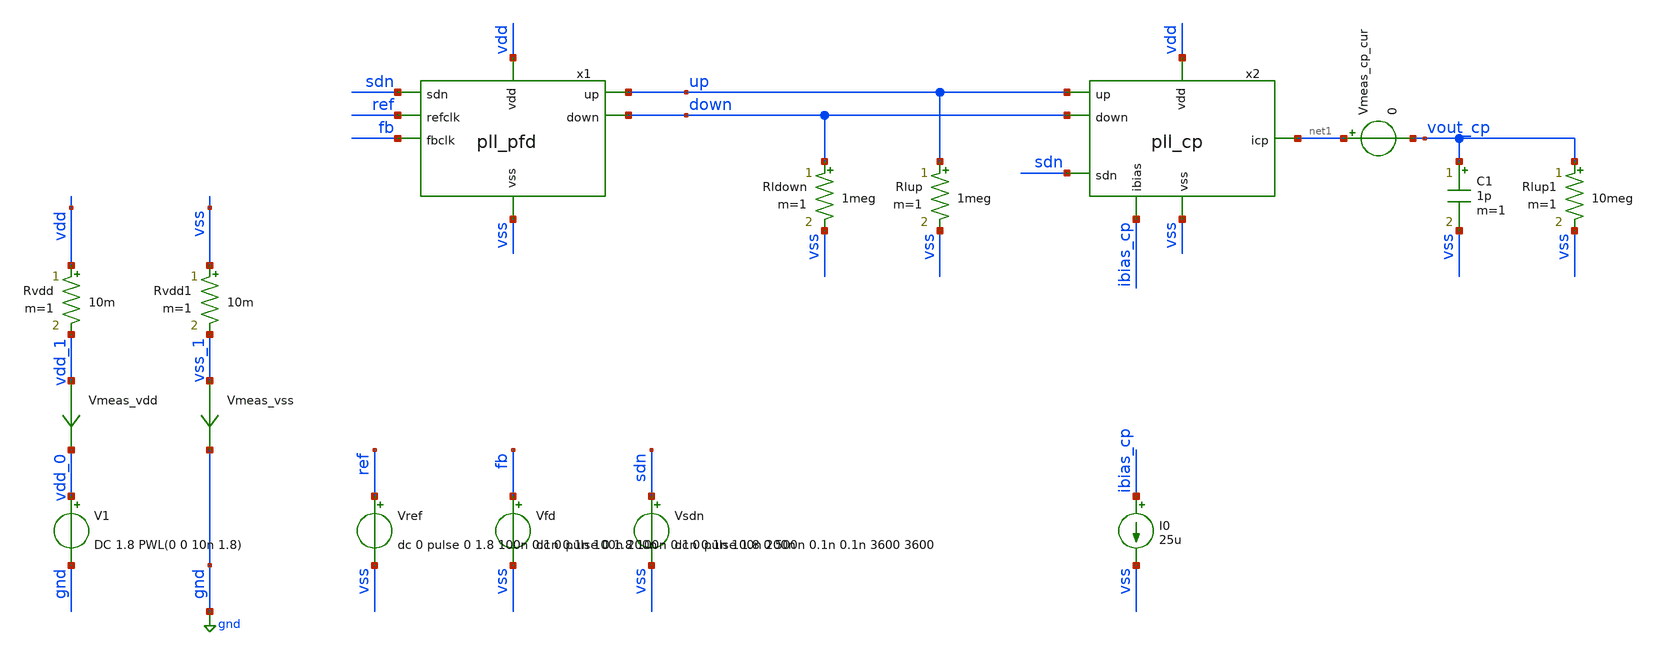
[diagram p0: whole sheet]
** sch_path: pll/pll_cp/simulation/pll_cp_tb.sch
**.subckt pll_cp_tb
V1 vdd_0 gnd DC 1.8 PWL(0 0 10n 1.8)
Vmeas_vdd vdd_1 vdd_0 0
.save i(vmeas_vdd)
Vref ref vss dc 0 pulse 0 1.8 100n 0.1n 0.1n 100n 200n
Vfd fb vss dc 0 pulse 0 1.8 100n 0.1n 0.1n 100n 200n
Vsdn sdn vss dc 0 pulse 1.8 0 500n 0.1n 0.1n 3600 3600
Vmeas_vss vss_1 gnd 0
.save i(vmeas_vss)
Rvdd vdd vdd_1 10m m=1
Rvdd1 vss vss_1 10m m=1
Rlup up vss 1meg m=1
Rldown down vss 1meg m=1
I0 ibias_cp vss 25u
Vmeas_cp_cur net1 vout_cp 0
Rlup1 vout_cp vss 10meg m=1
C1 vout_cp vss 1p m=1
x1 ref up sdn fb down vdd vss pll_pfd
x2 vdd up net1 ibias_cp down sdn vss pll_cp
**** begin user architecture code



.option savecurrents
*.option rshunt = 1e12
*.option gmin = 1e-24

** Settings for PSS osciallator
*.option reltol=1e-5
*.option vntol=3e-8
*.option abstol=1e-13
**.option chgtol=1e-12
*.option trtol=10
.option method=gear

.control

* #################################################################
* #
* #                         OPERATING POINT
* #
* #################################################################
reset
save all

op
set filetype=binary
write pll_cp_tb.raw all

* #################################################################
* #
* #                 TRANSIENT OSCILATION REGIME
* #
* #################################################################
reset
setplot const
save all
save v(ref)
save v(fb)
save v(sdn)
save v(up) v(up2)
save v(vout_cp)
save i(Vmeas_cp_cur)
save i(v.x2.Vcp1) i(v.x2.Vcp2)

tran 0.05n 2u uic
set filetype=ascii
write pll_cp_tb_tran.raw v(ref) v(fb) v(sdn) v(up) v(down)

* Plot outputs
plot v(sdn)+10 v(ref)+8 v(fb)+6 v(up)+4 v(down)+2 v(vout_cp)

*rusage
.endc



.options wnflag=1
.include $::SKYWATER_MODELS/cells/nfet_01v8/sky130_fd_pr__nfet_01v8__tt.corner.spice
.include $::SKYWATER_MODELS/cells/nfet_01v8_lvt/sky130_fd_pr__nfet_01v8_lvt__tt.corner.spice
.include $::SKYWATER_MODELS/cells/pfet_01v8/sky130_fd_pr__pfet_01v8__tt.corner.spice
.include $::SKYWATER_MODELS/cells/nfet_03v3_nvt/sky130_fd_pr__nfet_03v3_nvt__tt.corner.spice
.include $::SKYWATER_MODELS/cells/nfet_05v0_nvt/sky130_fd_pr__nfet_05v0_nvt__tt.corner.spice
.include $::SKYWATER_MODELS/cells/esd_nfet_01v8/sky130_fd_pr__esd_nfet_01v8__tt.corner.spice
.include $::SKYWATER_MODELS/cells/pfet_01v8_lvt/sky130_fd_pr__pfet_01v8_lvt__tt.corner.spice
.include $::SKYWATER_MODELS/cells/pfet_01v8_hvt/sky130_fd_pr__pfet_01v8_hvt__tt.corner.spice
.include $::SKYWATER_MODELS/cells/esd_pfet_g5v0d10v5/sky130_fd_pr__esd_pfet_g5v0d10v5__tt.corner.spice
.include $::SKYWATER_MODELS/cells/pfet_g5v0d10v5/sky130_fd_pr__pfet_g5v0d10v5__tt.corner.spice
.include $::SKYWATER_MODELS/cells/pfet_g5v0d16v0/sky130_fd_pr__pfet_g5v0d16v0__tt.corner.spice
.include $::SKYWATER_MODELS/cells/nfet_g5v0d10v5/sky130_fd_pr__nfet_g5v0d10v5__tt.corner.spice
.include $::SKYWATER_MODELS/cells/nfet_g5v0d16v0/sky130_fd_pr__nfet_g5v0d16v0__tt_discrete.corner.spice
.include $::SKYWATER_MODELS/cells/esd_nfet_g5v0d10v5/sky130_fd_pr__esd_nfet_g5v0d10v5__tt.corner.spice
.include $::SKYWATER_MODELS/models/corners/tt/nonfet.spice

.include $::SKYWATER_MODELS/cells/cap_var_hvt/sky130_fd_pr__cap_var_hvt.model.spice

* Mismatch parameters
.include $::SKYWATER_MODELS/cells/nfet_01v8/sky130_fd_pr__nfet_01v8__mismatch.corner.spice
.include $::SKYWATER_MODELS/cells/pfet_01v8/sky130_fd_pr__pfet_01v8__mismatch.corner.spice
.include $::SKYWATER_MODELS/cells/nfet_01v8_lvt/sky130_fd_pr__nfet_01v8_lvt__mismatch.corner.spice
.include $::SKYWATER_MODELS/cells/pfet_01v8_lvt/sky130_fd_pr__pfet_01v8_lvt__mismatch.corner.spice
.include $::SKYWATER_MODELS/cells/pfet_01v8_hvt/sky130_fd_pr__pfet_01v8_hvt__mismatch.corner.spice
.include $::SKYWATER_MODELS/cells/nfet_g5v0d10v5/sky130_fd_pr__nfet_g5v0d10v5__mismatch.corner.spice
.include $::SKYWATER_MODELS/cells/pfet_g5v0d10v5/sky130_fd_pr__pfet_g5v0d10v5__mismatch.corner.spice
.include $::SKYWATER_MODELS/cells/nfet_05v0_nvt/sky130_fd_pr__nfet_05v0_nvt__mismatch.corner.spice
.include $::SKYWATER_MODELS/cells/nfet_03v3_nvt/sky130_fd_pr__nfet_03v3_nvt__mismatch.corner.spice

* Resistor$::SKYWATER_MODELS/Capacitor
.include $::SKYWATER_MODELS/models/r+c/res_typical__cap_typical.spice
.include $::SKYWATER_MODELS/models/r+c/res_typical__cap_typical__lin.spice

* Special cells
.include $::SKYWATER_MODELS/models/corners/tt/specialized_cells.spice

* All models
.include $::SKYWATER_MODELS/models/all.spice

* Corner
.include $::SKYWATER_MODELS/models/corners/tt/rf.spice

* .include $::SKYWATER_STDCELLS/cells/
.include $::SKYWATER_STDCELLS/cells/buf/sky130_fd_sc_hd__buf_1.spice
.include $::SKYWATER_STDCELLS_HS/cells/buf/sky130_fd_sc_hs__buf_1.spice
.include $::SKYWATER_STDCELLS_HS/cells/buf/sky130_fd_sc_hs__buf_16.spice
.include $::SKYWATER_STDCELLS/cells/clkbuf/sky130_fd_sc_hd__clkbuf_1.spice
.include $::SKYWATER_STDCELLS/cells/clkbuf/sky130_fd_sc_hd__clkbuf_2.spice
.include $::SKYWATER_STDCELLS/cells/clkbuf/sky130_fd_sc_hd__clkbuf_4.spice
.include $::SKYWATER_STDCELLS/cells/clkbuf/sky130_fd_sc_hd__clkbuf_8.spice
.include $::SKYWATER_STDCELLS/cells/clkbuf/sky130_fd_sc_hd__clkbuf_16.spice
.include $::SKYWATER_STDCELLS/cells/decap/sky130_fd_sc_hd__decap_3.spice
.include $::SKYWATER_STDCELLS/cells/decap/sky130_fd_sc_hd__decap_4.spice
.include $::SKYWATER_STDCELLS/cells/decap/sky130_fd_sc_hd__decap_8.spice
.include $::SKYWATER_STDCELLS/cells/dfrbp/sky130_fd_sc_hd__dfrbp_1.spice
.include $::SKYWATER_STDCELLS/cells/dfrbp/sky130_fd_sc_hd__dfrbp_2.spice
.include $::SKYWATER_STDCELLS/cells/inv/sky130_fd_sc_hd__inv_1.spice
.include $::SKYWATER_STDCELLS/cells/inv/sky130_fd_sc_hd__inv_2.spice
.include $::SKYWATER_STDCELLS/cells/inv/sky130_fd_sc_hd__inv_4.spice
.include $::SKYWATER_STDCELLS/cells/inv/sky130_fd_sc_hd__inv_8.spice
.include $::SKYWATER_STDCELLS/cells/inv/sky130_fd_sc_hd__inv_16.spice
.include $::SKYWATER_STDCELLS_HS/cells/inv/sky130_fd_sc_hs__inv_1.spice
.include $::SKYWATER_STDCELLS_HS/cells/inv/sky130_fd_sc_hs__inv_2.spice
.include $::SKYWATER_STDCELLS_HS/cells/inv/sky130_fd_sc_hs__inv_4.spice
.include $::SKYWATER_STDCELLS_HS/cells/inv/sky130_fd_sc_hs__inv_8.spice
.include $::SKYWATER_STDCELLS_HS/cells/inv/sky130_fd_sc_hs__inv_16.spice
.include $::SKYWATER_STDCELLS/cells/mux2/sky130_fd_sc_hd__mux2_2.spice
.include $::SKYWATER_STDCELLS/cells/nand2/sky130_fd_sc_hd__nand2_1.spice
.include $::SKYWATER_STDCELLS/cells/tap/sky130_fd_sc_hd__tap_2.spice
.include $::SKYWATER_STDCELLS/cells/tapvpwrvgnd/sky130_fd_sc_hd__tapvpwrvgnd_1.spice

**** end user architecture code
**.ends

* expanding   symbol:  test_jens/pll/pll_pfd/pll_pfd.sym # of pins=7
** sym_path: pll/pll_pfd/xschem/pll_pfd.sym
** sch_path: pll/pll_pfd/xschem/pll_pfd.sch
.subckt pll_pfd refclk up sdn fbclk down vdd vss
*.ipin refclk
*.ipin fbclk
*.opin up
*.opin down
*.ipin sdn
*.ipin vdd
*.ipin vss
x1 refclk vdd rst_3 vss vss vdd vdd up up_inv sky130_fd_sc_hd__dfrbp_2
x2 fbclk vdd rst_3 vss vss vdd vdd down down_inv sky130_fd_sc_hd__dfrbp_2
x6 rst_2 sdn_inv vss vss vdd vdd rst_3 sky130_fd_sc_hd__and2_2
x4 rst_0 vss vss vdd vdd rst_1 sky130_fd_sc_hd__buf_1
x5 rst_1 vss vss vdd vdd rst_2 sky130_fd_sc_hd__buf_1
x7 sdn vss vss vdd vdd sdn_inv sky130_fd_sc_hd__inv_1
**** begin user architecture code
* .include $::SKYWATER_STDCELLS/cells/
.include $::SKYWATER_STDCELLS/cells/and2/sky130_fd_sc_hd__and2_1.spice
.include $::SKYWATER_STDCELLS/cells/and2/sky130_fd_sc_hd__and2_2.spice
.include $::SKYWATER_STDCELLS_HS/cells/and2/sky130_fd_sc_hs__and2_1.spice
.include $::SKYWATER_STDCELLS_HS/cells/and2/sky130_fd_sc_hs__and2_2.spice

.include $::SKYWATER_STDCELLS/cells/or2/sky130_fd_sc_hd__or2_1.spice
.include $::SKYWATER_STDCELLS/cells/or2/sky130_fd_sc_hd__or2_2.spice
.include $::SKYWATER_STDCELLS_HS/cells/or2/sky130_fd_sc_hs__or2_1.spice
.include $::SKYWATER_STDCELLS_HS/cells/or2/sky130_fd_sc_hs__or2_2.spice

.include $::SKYWATER_STDCELLS/cells/buf/sky130_fd_sc_hd__buf_1.spice
.include $::SKYWATER_STDCELLS_HS/cells/buf/sky130_fd_sc_hs__buf_1.spice

.include $::SKYWATER_STDCELLS/cells/dfrbp/sky130_fd_sc_hd__dfrbp_1.spice
.include $::SKYWATER_STDCELLS/cells/dfrbp/sky130_fd_sc_hd__dfrbp_2.spice
.include $::SKYWATER_STDCELLS_HS/cells/dfrbp/sky130_fd_sc_hs__dfrbp_1.spice
.include $::SKYWATER_STDCELLS_HS/cells/dfrbp/sky130_fd_sc_hs__dfrbp_2.spice

.include $::SKYWATER_STDCELLS/cells/inv/sky130_fd_sc_hd__inv_1.spice
.include $::SKYWATER_STDCELLS/cells/inv/sky130_fd_sc_hd__inv_2.spice
.include $::SKYWATER_STDCELLS/cells/inv/sky130_fd_sc_hd__inv_4.spice
.include $::SKYWATER_STDCELLS/cells/inv/sky130_fd_sc_hd__inv_8.spice
.include $::SKYWATER_STDCELLS/cells/inv/sky130_fd_sc_hd__inv_16.spice
.include $::SKYWATER_STDCELLS_HS/cells/inv/sky130_fd_sc_hs__inv_1.spice
.include $::SKYWATER_STDCELLS_HS/cells/inv/sky130_fd_sc_hs__inv_2.spice
.include $::SKYWATER_STDCELLS_HS/cells/inv/sky130_fd_sc_hs__inv_4.spice
.include $::SKYWATER_STDCELLS_HS/cells/inv/sky130_fd_sc_hs__inv_8.spice
.include $::SKYWATER_STDCELLS_HS/cells/inv/sky130_fd_sc_hs__inv_16.spice

.include $::SKYWATER_STDCELLS/cells/mux2/sky130_fd_sc_hd__mux2_2.spice
.include $::SKYWATER_STDCELLS/cells/nand2/sky130_fd_sc_hd__nand2_1.spice

.include $::SKYWATER_STDCELLS/cells/tap/sky130_fd_sc_hd__tap_2.spice
.include $::SKYWATER_STDCELLS/cells/tapvpwrvgnd/sky130_fd_sc_hd__tapvpwrvgnd_1.spice

**** end user architecture code
x3 up_inv down_inv vss vss vdd vdd rst_0 sky130_fd_sc_hd__or2_1
* noconn vss
* noconn vdd
.ends


* expanding   symbol:  test_jens/pll/pll_cp/pll_cp.sym # of pins=7
** sym_path: pll/pll_cp/xschem/pll_cp.sym
** sch_path: pll/pll_cp/xschem/pll_cp.sch
.subckt pll_cp vdd up icp ibias down sdn vss
*.ipin vdd
*.ipin vss
*.ipin up
*.ipin down
*.ipin ibias
*.ipin sdn
*.opin icp
**** begin user architecture code
* .include $::SKYWATER_STDCELLS/cells/
.include $::SKYWATER_STDCELLS/cells/and2/sky130_fd_sc_hd__and2_1.spice
.include $::SKYWATER_STDCELLS/cells/and2/sky130_fd_sc_hd__and2_2.spice
.include $::SKYWATER_STDCELLS_HS/cells/and2/sky130_fd_sc_hs__and2_1.spice
.include $::SKYWATER_STDCELLS_HS/cells/and2/sky130_fd_sc_hs__and2_2.spice

.include $::SKYWATER_STDCELLS/cells/or2/sky130_fd_sc_hd__or2_1.spice
.include $::SKYWATER_STDCELLS/cells/or2/sky130_fd_sc_hd__or2_2.spice
.include $::SKYWATER_STDCELLS_HS/cells/or2/sky130_fd_sc_hs__or2_1.spice
.include $::SKYWATER_STDCELLS_HS/cells/or2/sky130_fd_sc_hs__or2_2.spice

.include $::SKYWATER_STDCELLS/cells/buf/sky130_fd_sc_hd__buf_1.spice
.include $::SKYWATER_STDCELLS_HS/cells/buf/sky130_fd_sc_hs__buf_1.spice

.include $::SKYWATER_STDCELLS/cells/dfrbp/sky130_fd_sc_hd__dfrbp_1.spice
.include $::SKYWATER_STDCELLS/cells/dfrbp/sky130_fd_sc_hd__dfrbp_2.spice
.include $::SKYWATER_STDCELLS_HS/cells/dfrbp/sky130_fd_sc_hs__dfrbp_1.spice
.include $::SKYWATER_STDCELLS_HS/cells/dfrbp/sky130_fd_sc_hs__dfrbp_2.spice

.include $::SKYWATER_STDCELLS/cells/inv/sky130_fd_sc_hd__inv_1.spice
.include $::SKYWATER_STDCELLS/cells/inv/sky130_fd_sc_hd__inv_2.spice
.include $::SKYWATER_STDCELLS/cells/inv/sky130_fd_sc_hd__inv_4.spice
.include $::SKYWATER_STDCELLS/cells/inv/sky130_fd_sc_hd__inv_8.spice
.include $::SKYWATER_STDCELLS/cells/inv/sky130_fd_sc_hd__inv_16.spice
.include $::SKYWATER_STDCELLS_HS/cells/inv/sky130_fd_sc_hs__inv_1.spice
.include $::SKYWATER_STDCELLS_HS/cells/inv/sky130_fd_sc_hs__inv_2.spice
.include $::SKYWATER_STDCELLS_HS/cells/inv/sky130_fd_sc_hs__inv_4.spice
.include $::SKYWATER_STDCELLS_HS/cells/inv/sky130_fd_sc_hs__inv_8.spice
.include $::SKYWATER_STDCELLS_HS/cells/inv/sky130_fd_sc_hs__inv_16.spice

.include $::SKYWATER_STDCELLS/cells/mux2/sky130_fd_sc_hd__mux2_2.spice
.include $::SKYWATER_STDCELLS/cells/nand2/sky130_fd_sc_hd__nand2_1.spice

.include $::SKYWATER_STDCELLS/cells/tap/sky130_fd_sc_hd__tap_2.spice
.include $::SKYWATER_STDCELLS/cells/tapvpwrvgnd/sky130_fd_sc_hd__tapvpwrvgnd_1.spice

**** end user architecture code
XM1 net1 vgn1 vss vss sky130_fd_pr__nfet_01v8 L=0.15 W=4 nf=8 ad='int((nf+1)/2) * W/nf * 0.29' as='int((nf+2)/2) * W/nf * 0.29'
+ pd='2*int((nf+1)/2) * (W/nf + 0.29)' ps='2*int((nf+2)/2) * (W/nf + 0.29)' nrd='0.29 / W' nrs='0.29 / W'
+ sa=0 sb=0 sd=0 mult=1 m=1
XM2 vgn1 vgn2 net1 vss sky130_fd_pr__nfet_01v8 L=0.15 W=4 nf=8 ad='int((nf+1)/2) * W/nf * 0.29' as='int((nf+2)/2) * W/nf * 0.29'
+ pd='2*int((nf+1)/2) * (W/nf + 0.29)' ps='2*int((nf+2)/2) * (W/nf + 0.29)' nrd='0.29 / W' nrs='0.29 / W'
+ sa=0 sb=0 sd=0 mult=1 m=1
XM3 net2 vgn1 vss vss sky130_fd_pr__nfet_01v8 L=0.15 W=4 nf=8 ad='int((nf+1)/2) * W/nf * 0.29' as='int((nf+2)/2) * W/nf * 0.29'
+ pd='2*int((nf+1)/2) * (W/nf + 0.29)' ps='2*int((nf+2)/2) * (W/nf + 0.29)' nrd='0.29 / W' nrs='0.29 / W'
+ sa=0 sb=0 sd=0 mult=1 m=1
XM4 vgn2 vgn2 net2 vss sky130_fd_pr__nfet_01v8 L=0.15 W=4 nf=8 ad='int((nf+1)/2) * W/nf * 0.29' as='int((nf+2)/2) * W/nf * 0.29'
+ pd='2*int((nf+1)/2) * (W/nf + 0.29)' ps='2*int((nf+2)/2) * (W/nf + 0.29)' nrd='0.29 / W' nrs='0.29 / W'
+ sa=0 sb=0 sd=0 mult=1 m=1
XM5 net3 net4 vdd vdd sky130_fd_pr__pfet_01v8 L=0.15 W=12 nf=8 ad='int((nf+1)/2) * W/nf * 0.29' as='int((nf+2)/2) * W/nf * 0.29'
+ pd='2*int((nf+1)/2) * (W/nf + 0.29)' ps='2*int((nf+2)/2) * (W/nf + 0.29)' nrd='0.29 / W' nrs='0.29 / W'
+ sa=0 sb=0 sd=0 mult=1 m=1
XM6 net4 vgp2 net3 vdd sky130_fd_pr__pfet_01v8 L=0.15 W=12 nf=8 ad='int((nf+1)/2) * W/nf * 0.29' as='int((nf+2)/2) * W/nf * 0.29'
+ pd='2*int((nf+1)/2) * (W/nf + 0.29)' ps='2*int((nf+2)/2) * (W/nf + 0.29)' nrd='0.29 / W' nrs='0.29 / W'
+ sa=0 sb=0 sd=0 mult=1 m=1
XM7 net5 vgp1 vdd vdd sky130_fd_pr__pfet_01v8 L=0.15 W=12 nf=8 ad='int((nf+1)/2) * W/nf * 0.29' as='int((nf+2)/2) * W/nf * 0.29'
+ pd='2*int((nf+1)/2) * (W/nf + 0.29)' ps='2*int((nf+2)/2) * (W/nf + 0.29)' nrd='0.29 / W' nrs='0.29 / W'
+ sa=0 sb=0 sd=0 mult=1 m=1
XM8 vgp2 vgp2 net5 vdd sky130_fd_pr__pfet_01v8 L=0.15 W=12 nf=8 ad='int((nf+1)/2) * W/nf * 0.29' as='int((nf+2)/2) * W/nf * 0.29'
+ pd='2*int((nf+1)/2) * (W/nf + 0.29)' ps='2*int((nf+2)/2) * (W/nf + 0.29)' nrd='0.29 / W' nrs='0.29 / W'
+ sa=0 sb=0 sd=0 mult=1 m=1
XM9 net6 net6 vdd vdd sky130_fd_pr__pfet_01v8 L=0.15 W=12 nf=8 ad='int((nf+1)/2) * W/nf * 0.29' as='int((nf+2)/2) * W/nf * 0.29'
+ pd='2*int((nf+1)/2) * (W/nf + 0.29)' ps='2*int((nf+2)/2) * (W/nf + 0.29)' nrd='0.29 / W' nrs='0.29 / W'
+ sa=0 sb=0 sd=0 mult=1 m=1
XM10 net17 sdn net6 vdd sky130_fd_pr__pfet_01v8 L=0.15 W=12 nf=8 ad='int((nf+1)/2) * W/nf * 0.29' as='int((nf+2)/2) * W/nf * 0.29'
+ pd='2*int((nf+1)/2) * (W/nf + 0.29)' ps='2*int((nf+2)/2) * (W/nf + 0.29)' nrd='0.29 / W' nrs='0.29 / W'
+ sa=0 sb=0 sd=0 mult=1 m=1
XM11 net7 vgn1 vss vss sky130_fd_pr__nfet_01v8 L=0.15 W=4 nf=8 ad='int((nf+1)/2) * W/nf * 0.29' as='int((nf+2)/2) * W/nf * 0.29'
+ pd='2*int((nf+1)/2) * (W/nf + 0.29)' ps='2*int((nf+2)/2) * (W/nf + 0.29)' nrd='0.29 / W' nrs='0.29 / W'
+ sa=0 sb=0 sd=0 mult=1 m=1
XM12 net11 vgn2 net7 vss sky130_fd_pr__nfet_01v8 L=0.15 W=4 nf=8 ad='int((nf+1)/2) * W/nf * 0.29' as='int((nf+2)/2) * W/nf * 0.29'
+ pd='2*int((nf+1)/2) * (W/nf + 0.29)' ps='2*int((nf+2)/2) * (W/nf + 0.29)' nrd='0.29 / W' nrs='0.29 / W'
+ sa=0 sb=0 sd=0 mult=1 m=1
XM13 net8 vgn1 vdd vdd sky130_fd_pr__pfet_01v8 L=0.15 W=12 nf=8 ad='int((nf+1)/2) * W/nf * 0.29' as='int((nf+2)/2) * W/nf * 0.29'
+ pd='2*int((nf+1)/2) * (W/nf + 0.29)' ps='2*int((nf+2)/2) * (W/nf + 0.29)' nrd='0.29 / W' nrs='0.29 / W'
+ sa=0 sb=0 sd=0 mult=1 m=1
XM14 net10 vgn2 net8 vdd sky130_fd_pr__pfet_01v8 L=0.15 W=12 nf=8 ad='int((nf+1)/2) * W/nf * 0.29' as='int((nf+2)/2) * W/nf * 0.29'
+ pd='2*int((nf+1)/2) * (W/nf + 0.29)' ps='2*int((nf+2)/2) * (W/nf + 0.29)' nrd='0.29 / W' nrs='0.29 / W'
+ sa=0 sb=0 sd=0 mult=1 m=1
XM15 vgp1 sdnb vdd vdd sky130_fd_pr__pfet_01v8 L=0.15 W=0.5 nf=1 ad='int((nf+1)/2) * W/nf * 0.29' as='int((nf+2)/2) * W/nf * 0.29'
+ pd='2*int((nf+1)/2) * (W/nf + 0.29)' ps='2*int((nf+2)/2) * (W/nf + 0.29)' nrd='0.29 / W' nrs='0.29 / W'
+ sa=0 sb=0 sd=0 mult=1 m=1
XM16 vgp2 sdnb vdd vdd sky130_fd_pr__pfet_01v8 L=0.15 W=0.5 nf=1 ad='int((nf+1)/2) * W/nf * 0.29' as='int((nf+2)/2) * W/nf * 0.29'
+ pd='2*int((nf+1)/2) * (W/nf + 0.29)' ps='2*int((nf+2)/2) * (W/nf + 0.29)' nrd='0.29 / W' nrs='0.29 / W'
+ sa=0 sb=0 sd=0 mult=1 m=1
XM17 vgn1 sdn vss vss sky130_fd_pr__nfet_01v8 L=0.15 W=0.5 nf=1 ad='int((nf+1)/2) * W/nf * 0.29' as='int((nf+2)/2) * W/nf * 0.29'
+ pd='2*int((nf+1)/2) * (W/nf + 0.29)' ps='2*int((nf+2)/2) * (W/nf + 0.29)' nrd='0.29 / W' nrs='0.29 / W'
+ sa=0 sb=0 sd=0 mult=1 m=1
XM18 vgn2 sdn vss vss sky130_fd_pr__nfet_01v8 L=0.15 W=0.5 nf=1 ad='int((nf+1)/2) * W/nf * 0.29' as='int((nf+2)/2) * W/nf * 0.29'
+ pd='2*int((nf+1)/2) * (W/nf + 0.29)' ps='2*int((nf+2)/2) * (W/nf + 0.29)' nrd='0.29 / W' nrs='0.29 / W'
+ sa=0 sb=0 sd=0 mult=1 m=1
x5 sdn vss vss vdd vdd sdnb sky130_fd_sc_hd__inv_1
XM19 vgn1 sdn net16 vdd sky130_fd_pr__pfet_01v8 L=0.15 W=12 nf=8 ad='int((nf+1)/2) * W/nf * 0.29' as='int((nf+2)/2) * W/nf * 0.29'
+ pd='2*int((nf+1)/2) * (W/nf + 0.29)' ps='2*int((nf+2)/2) * (W/nf + 0.29)' nrd='0.29 / W' nrs='0.29 / W'
+ sa=0 sb=0 sd=0 mult=1 m=1
XM20 ibias sdn net9 vdd sky130_fd_pr__pfet_01v8 L=0.15 W=12 nf=8 ad='int((nf+1)/2) * W/nf * 0.29' as='int((nf+2)/2) * W/nf * 0.29'
+ pd='2*int((nf+1)/2) * (W/nf + 0.29)' ps='2*int((nf+2)/2) * (W/nf + 0.29)' nrd='0.29 / W' nrs='0.29 / W'
+ sa=0 sb=0 sd=0 mult=1 m=1
XM21 net9 sdnb ibias vss sky130_fd_pr__nfet_01v8 L=0.15 W=4 nf=8 ad='int((nf+1)/2) * W/nf * 0.29' as='int((nf+2)/2) * W/nf * 0.29'
+ pd='2*int((nf+1)/2) * (W/nf + 0.29)' ps='2*int((nf+2)/2) * (W/nf + 0.29)' nrd='0.29 / W' nrs='0.29 / W'
+ sa=0 sb=0 sd=0 mult=1 m=1
R1 vgp1 net4 10m m=1
Vmeas net4 net9 0
.save i(vmeas)
Vmeas1 vgp2 net16 0
.save i(vmeas1)
Vmeas2 net17 vgn2 0
.save i(vmeas2)
E1 icp_bias vss icp vss 1
x1 vdd net12 net13 up net14 net15 vss pll_cp_sw_clk_gen
x2 vdd net18 net19 down net20 net21 vss pll_cp_sw_clk_gen
x3 net10 net12 net13 net14 net15 vdd icp_bias icp vss pll_cp_sw_spdt
x4 net11 net21 net20 net19 net18 vdd icp_bias icp vss pll_cp_sw_spdt
.ends


* expanding   symbol:  pll_cp_sw_clk_gen/xschem/pll_cp_sw_clk_gen.sym # of pins=7
** sym_path: pll/pll_cp_sw_clk_gen/xschem/pll_cp_sw_clk_gen.sym
** sch_path: pll/pll_cp_sw_clk_gen/xschem/pll_cp_sw_clk_gen.sch
.subckt pll_cp_sw_clk_gen vdd phase1 phase1b clk_in phase2 phase2b vss
*.ipin vdd
*.ipin vss
*.ipin clk_in
*.opin phase1
*.opin phase1b
*.opin phase2
*.opin phase2b
x1 net1 vdd vss clk_in net2 pll_nol_clkb
x2 phase2 vdd vss net2 phase2b pll_sync_clkb
x3 phase1 vdd vss net1 phase1b pll_sync_clkb
.ends


* expanding   symbol:  pll_cp_sw_spdt/xschem/pll_cp_sw_spdt.sym # of pins=9
** sym_path: pll/pll_cp_sw_spdt/xschem/pll_cp_sw_spdt.sym
** sch_path: pll/pll_cp_sw_spdt/xschem/pll_cp_sw_spdt.sch
.subckt pll_cp_sw_spdt cm phase1 phase1b phase2 phase2b vdd out1 out2 vss
*.ipin vdd
*.ipin vss
*.ipin phase1
*.ipin phase1b
*.ipin phase2
*.ipin phase2b
*.ipin cm
*.opin out2
*.opin out1
XM1 cm phase1 out1 vss sky130_fd_pr__nfet_01v8 L=0.15 W=2 nf=1 ad='int((nf+1)/2) * W/nf * 0.29' as='int((nf+2)/2) * W/nf * 0.29'
+ pd='2*int((nf+1)/2) * (W/nf + 0.29)' ps='2*int((nf+2)/2) * (W/nf + 0.29)' nrd='0.29 / W' nrs='0.29 / W'
+ sa=0 sb=0 sd=0 mult=1 m=1
XM2 cm phase1b out1 vdd sky130_fd_pr__pfet_01v8 L=0.15 W=4 nf=1 ad='int((nf+1)/2) * W/nf * 0.29' as='int((nf+2)/2) * W/nf * 0.29'
+ pd='2*int((nf+1)/2) * (W/nf + 0.29)' ps='2*int((nf+2)/2) * (W/nf + 0.29)' nrd='0.29 / W' nrs='0.29 / W'
+ sa=0 sb=0 sd=0 mult=1 m=1
XM3 cm phase2 out2 vss sky130_fd_pr__nfet_01v8 L=0.15 W=2 nf=1 ad='int((nf+1)/2) * W/nf * 0.29' as='int((nf+2)/2) * W/nf * 0.29'
+ pd='2*int((nf+1)/2) * (W/nf + 0.29)' ps='2*int((nf+2)/2) * (W/nf + 0.29)' nrd='0.29 / W' nrs='0.29 / W'
+ sa=0 sb=0 sd=0 mult=1 m=1
XM4 cm phase2b out2 vdd sky130_fd_pr__pfet_01v8 L=0.15 W=4 nf=1 ad='int((nf+1)/2) * W/nf * 0.29' as='int((nf+2)/2) * W/nf * 0.29'
+ pd='2*int((nf+1)/2) * (W/nf + 0.29)' ps='2*int((nf+2)/2) * (W/nf + 0.29)' nrd='0.29 / W' nrs='0.29 / W'
+ sa=0 sb=0 sd=0 mult=1 m=1
.ends


* expanding   symbol:  pll_nol_clkb/xschem/pll_nol_clkb.sym # of pins=5
** sym_path: pll/pll_nol_clkb/xschem/pll_nol_clkb.sym
** sch_path: pll/pll_nol_clkb/xschem/pll_nol_clkb.sch
.subckt pll_nol_clkb clk1 vdd vss clk clk2
*.opin clk1
*.opin clk2
*.ipin vdd
*.ipin vss
*.ipin clk
**** begin user architecture code
* .include $::SKYWATER_STDCELLS/cells/
.include $::SKYWATER_STDCELLS/cells/and2/sky130_fd_sc_hd__and2_1.spice
.include $::SKYWATER_STDCELLS/cells/and2/sky130_fd_sc_hd__and2_2.spice
.include $::SKYWATER_STDCELLS_HS/cells/and2/sky130_fd_sc_hs__and2_1.spice
.include $::SKYWATER_STDCELLS_HS/cells/and2/sky130_fd_sc_hs__and2_2.spice

.include $::SKYWATER_STDCELLS/cells/nand2/sky130_fd_sc_hd__nand2_1.spice
.include $::SKYWATER_STDCELLS/cells/nand2/sky130_fd_sc_hd__nand2_2.spice
.include $::SKYWATER_STDCELLS_HS/cells/nand2/sky130_fd_sc_hs__nand2_1.spice
.include $::SKYWATER_STDCELLS_HS/cells/nand2/sky130_fd_sc_hs__nand2_2.spice

.include $::SKYWATER_STDCELLS/cells/or2/sky130_fd_sc_hd__or2_1.spice
.include $::SKYWATER_STDCELLS/cells/or2/sky130_fd_sc_hd__or2_2.spice
.include $::SKYWATER_STDCELLS_HS/cells/or2/sky130_fd_sc_hs__or2_1.spice
.include $::SKYWATER_STDCELLS_HS/cells/or2/sky130_fd_sc_hs__or2_2.spice

.include $::SKYWATER_STDCELLS/cells/buf/sky130_fd_sc_hd__buf_1.spice
.include $::SKYWATER_STDCELLS_HS/cells/buf/sky130_fd_sc_hs__buf_1.spice

.include $::SKYWATER_STDCELLS/cells/dfrbp/sky130_fd_sc_hd__dfrbp_1.spice
.include $::SKYWATER_STDCELLS/cells/dfrbp/sky130_fd_sc_hd__dfrbp_2.spice
.include $::SKYWATER_STDCELLS_HS/cells/dfrbp/sky130_fd_sc_hs__dfrbp_1.spice
.include $::SKYWATER_STDCELLS_HS/cells/dfrbp/sky130_fd_sc_hs__dfrbp_2.spice

.include $::SKYWATER_STDCELLS/cells/inv/sky130_fd_sc_hd__inv_1.spice
.include $::SKYWATER_STDCELLS/cells/inv/sky130_fd_sc_hd__inv_2.spice
.include $::SKYWATER_STDCELLS/cells/inv/sky130_fd_sc_hd__inv_4.spice
.include $::SKYWATER_STDCELLS/cells/inv/sky130_fd_sc_hd__inv_8.spice
.include $::SKYWATER_STDCELLS/cells/inv/sky130_fd_sc_hd__inv_16.spice
.include $::SKYWATER_STDCELLS_HS/cells/inv/sky130_fd_sc_hs__inv_1.spice
.include $::SKYWATER_STDCELLS_HS/cells/inv/sky130_fd_sc_hs__inv_2.spice
.include $::SKYWATER_STDCELLS_HS/cells/inv/sky130_fd_sc_hs__inv_4.spice
.include $::SKYWATER_STDCELLS_HS/cells/inv/sky130_fd_sc_hs__inv_8.spice
.include $::SKYWATER_STDCELLS_HS/cells/inv/sky130_fd_sc_hs__inv_16.spice

.include $::SKYWATER_STDCELLS/cells/mux2/sky130_fd_sc_hd__mux2_2.spice
.include $::SKYWATER_STDCELLS/cells/nand2/sky130_fd_sc_hd__nand2_1.spice

.include $::SKYWATER_STDCELLS/cells/tap/sky130_fd_sc_hd__tap_2.spice
.include $::SKYWATER_STDCELLS/cells/tapvpwrvgnd/sky130_fd_sc_hd__tapvpwrvgnd_1.spice

**** end user architecture code
x3 clk1b vss vss vdd vdd clk1 sky130_fd_sc_hd__inv_1
x4 clk1 vss vss vdd vdd clk1fb sky130_fd_sc_hd__inv_1
x5 clk2b vss vss vdd vdd clk2 sky130_fd_sc_hd__inv_1
x6 clk2 vss vss vdd vdd clk2fb sky130_fd_sc_hd__inv_1
x7 clk vss vss vdd vdd clkb sky130_fd_sc_hd__inv_1
x1 clkb clk2fb vss vss vdd vdd clk1b sky130_fd_sc_hd__nand2_2
x2 clk1fb clk vss vss vdd vdd clk2b sky130_fd_sc_hd__nand2_2
* noconn vdd
* noconn vss
.ends


* expanding   symbol:  pll_sync_clkb/xschem/pll_sync_clkb.sym # of pins=5
** sym_path: pll/pll_sync_clkb/xschem/pll_sync_clkb.sym
** sch_path: pll/pll_sync_clkb/xschem/pll_sync_clkb.sch
.subckt pll_sync_clkb out_clk vdd vss in_clk out_clkb
*.opin out_clk
*.opin out_clkb
*.ipin vdd
*.ipin vss
*.ipin in_clk
**** begin user architecture code
* .include $::SKYWATER_STDCELLS/cells/
.include $::SKYWATER_STDCELLS/cells/and2/sky130_fd_sc_hd__and2_1.spice
.include $::SKYWATER_STDCELLS/cells/and2/sky130_fd_sc_hd__and2_2.spice
.include $::SKYWATER_STDCELLS_HS/cells/and2/sky130_fd_sc_hs__and2_1.spice
.include $::SKYWATER_STDCELLS_HS/cells/and2/sky130_fd_sc_hs__and2_2.spice

.include $::SKYWATER_STDCELLS/cells/nand2/sky130_fd_sc_hd__nand2_1.spice
.include $::SKYWATER_STDCELLS/cells/nand2/sky130_fd_sc_hd__nand2_2.spice
.include $::SKYWATER_STDCELLS_HS/cells/nand2/sky130_fd_sc_hs__nand2_1.spice
.include $::SKYWATER_STDCELLS_HS/cells/nand2/sky130_fd_sc_hs__nand2_2.spice

.include $::SKYWATER_STDCELLS/cells/or2/sky130_fd_sc_hd__or2_1.spice
.include $::SKYWATER_STDCELLS/cells/or2/sky130_fd_sc_hd__or2_2.spice
.include $::SKYWATER_STDCELLS_HS/cells/or2/sky130_fd_sc_hs__or2_1.spice
.include $::SKYWATER_STDCELLS_HS/cells/or2/sky130_fd_sc_hs__or2_2.spice

.include $::SKYWATER_STDCELLS/cells/buf/sky130_fd_sc_hd__buf_1.spice
.include $::SKYWATER_STDCELLS_HS/cells/buf/sky130_fd_sc_hs__buf_1.spice

.include $::SKYWATER_STDCELLS/cells/dfrbp/sky130_fd_sc_hd__dfrbp_1.spice
.include $::SKYWATER_STDCELLS/cells/dfrbp/sky130_fd_sc_hd__dfrbp_2.spice
.include $::SKYWATER_STDCELLS_HS/cells/dfrbp/sky130_fd_sc_hs__dfrbp_1.spice
.include $::SKYWATER_STDCELLS_HS/cells/dfrbp/sky130_fd_sc_hs__dfrbp_2.spice

.include $::SKYWATER_STDCELLS/cells/inv/sky130_fd_sc_hd__inv_1.spice
.include $::SKYWATER_STDCELLS/cells/inv/sky130_fd_sc_hd__inv_2.spice
.include $::SKYWATER_STDCELLS/cells/inv/sky130_fd_sc_hd__inv_4.spice
.include $::SKYWATER_STDCELLS/cells/inv/sky130_fd_sc_hd__inv_8.spice
.include $::SKYWATER_STDCELLS/cells/inv/sky130_fd_sc_hd__inv_16.spice
.include $::SKYWATER_STDCELLS_HS/cells/inv/sky130_fd_sc_hs__inv_1.spice
.include $::SKYWATER_STDCELLS_HS/cells/inv/sky130_fd_sc_hs__inv_2.spice
.include $::SKYWATER_STDCELLS_HS/cells/inv/sky130_fd_sc_hs__inv_4.spice
.include $::SKYWATER_STDCELLS_HS/cells/inv/sky130_fd_sc_hs__inv_8.spice
.include $::SKYWATER_STDCELLS_HS/cells/inv/sky130_fd_sc_hs__inv_16.spice

.include $::SKYWATER_STDCELLS/cells/mux2/sky130_fd_sc_hd__mux2_2.spice
.include $::SKYWATER_STDCELLS/cells/nand2/sky130_fd_sc_hd__nand2_1.spice

.include $::SKYWATER_STDCELLS/cells/tap/sky130_fd_sc_hd__tap_2.spice
.include $::SKYWATER_STDCELLS/cells/tapvpwrvgnd/sky130_fd_sc_hd__tapvpwrvgnd_1.spice

**** end user architecture code
x1 in_clk vss vss vdd vdd net1 sky130_fd_sc_hd__inv_2
x2 net1 vss vss vdd vdd net2 sky130_fd_sc_hd__inv_2
x4 stor_node vss vss vdd vdd out_clk sky130_fd_sc_hd__inv_1
x6 stor_node_b vss vss vdd vdd out_clkb sky130_fd_sc_hd__inv_1
x7 stor_node_b vss vss vdd vdd stor_node sky130_fd_sc_hd__inv_2
x9 stor_node vss vss vdd vdd stor_node_b sky130_fd_sc_hd__inv_2
x3 net2 vss vss vdd vdd stor_node sky130_fd_sc_hd__inv_1
x5 net1 vss vss vdd vdd stor_node_b sky130_fd_sc_hd__inv_1
* noconn vdd
* noconn vss
.ends

.GLOBAL gnd
.end
